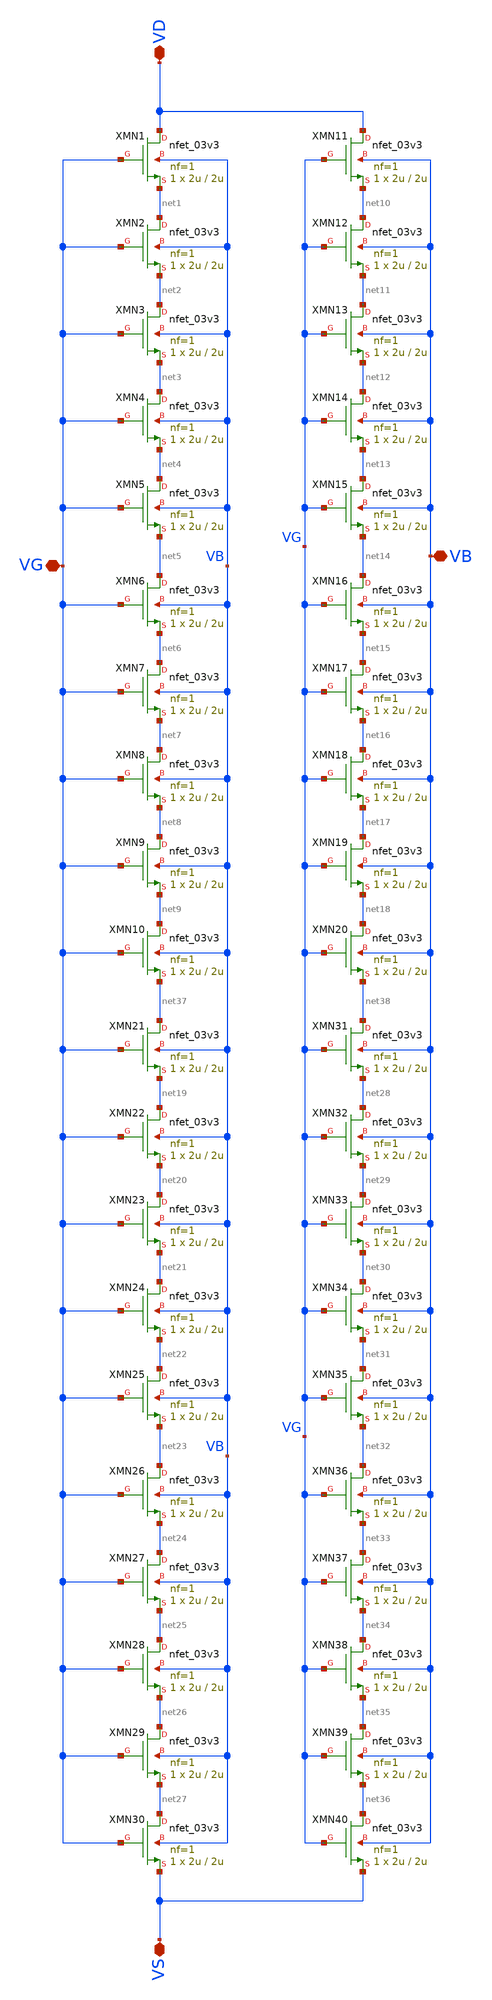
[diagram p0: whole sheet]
** sch_path: Voltage_Reference/symbols_vr/10_NMOS_series.sch
**.subckt 10_NMOS_series VD VG VS VB
*.iopin VD
*.iopin VG
*.iopin VS
*.iopin VB
XMN1 VD VG net1 VB nfet_03v3 L=2u W=2u nf=1 ad='int((nf+1)/2) * W/nf * 0.18u' as='int((nf+2)/2) * W/nf * 0.18u'
+ pd='2*int((nf+1)/2) * (W/nf + 0.18u)' ps='2*int((nf+2)/2) * (W/nf + 0.18u)' nrd='0.18u / W' nrs='0.18u / W'
+ sa=0 sb=0 sd=0 m=1
XMN2 net1 VG net2 VB nfet_03v3 L=2u W=2u nf=1 ad='int((nf+1)/2) * W/nf * 0.18u' as='int((nf+2)/2) * W/nf * 0.18u'
+ pd='2*int((nf+1)/2) * (W/nf + 0.18u)' ps='2*int((nf+2)/2) * (W/nf + 0.18u)' nrd='0.18u / W' nrs='0.18u / W'
+ sa=0 sb=0 sd=0 m=1
XMN3 net2 VG net3 VB nfet_03v3 L=2u W=2u nf=1 ad='int((nf+1)/2) * W/nf * 0.18u' as='int((nf+2)/2) * W/nf * 0.18u'
+ pd='2*int((nf+1)/2) * (W/nf + 0.18u)' ps='2*int((nf+2)/2) * (W/nf + 0.18u)' nrd='0.18u / W' nrs='0.18u / W'
+ sa=0 sb=0 sd=0 m=1
XMN4 net3 VG net4 VB nfet_03v3 L=2u W=2u nf=1 ad='int((nf+1)/2) * W/nf * 0.18u' as='int((nf+2)/2) * W/nf * 0.18u'
+ pd='2*int((nf+1)/2) * (W/nf + 0.18u)' ps='2*int((nf+2)/2) * (W/nf + 0.18u)' nrd='0.18u / W' nrs='0.18u / W'
+ sa=0 sb=0 sd=0 m=1
XMN5 net4 VG net5 VB nfet_03v3 L=2u W=2u nf=1 ad='int((nf+1)/2) * W/nf * 0.18u' as='int((nf+2)/2) * W/nf * 0.18u'
+ pd='2*int((nf+1)/2) * (W/nf + 0.18u)' ps='2*int((nf+2)/2) * (W/nf + 0.18u)' nrd='0.18u / W' nrs='0.18u / W'
+ sa=0 sb=0 sd=0 m=1
XMN6 net5 VG net6 VB nfet_03v3 L=2u W=2u nf=1 ad='int((nf+1)/2) * W/nf * 0.18u' as='int((nf+2)/2) * W/nf * 0.18u'
+ pd='2*int((nf+1)/2) * (W/nf + 0.18u)' ps='2*int((nf+2)/2) * (W/nf + 0.18u)' nrd='0.18u / W' nrs='0.18u / W'
+ sa=0 sb=0 sd=0 m=1
XMN7 net6 VG net7 VB nfet_03v3 L=2u W=2u nf=1 ad='int((nf+1)/2) * W/nf * 0.18u' as='int((nf+2)/2) * W/nf * 0.18u'
+ pd='2*int((nf+1)/2) * (W/nf + 0.18u)' ps='2*int((nf+2)/2) * (W/nf + 0.18u)' nrd='0.18u / W' nrs='0.18u / W'
+ sa=0 sb=0 sd=0 m=1
XMN8 net7 VG net8 VB nfet_03v3 L=2u W=2u nf=1 ad='int((nf+1)/2) * W/nf * 0.18u' as='int((nf+2)/2) * W/nf * 0.18u'
+ pd='2*int((nf+1)/2) * (W/nf + 0.18u)' ps='2*int((nf+2)/2) * (W/nf + 0.18u)' nrd='0.18u / W' nrs='0.18u / W'
+ sa=0 sb=0 sd=0 m=1
XMN9 net8 VG net9 VB nfet_03v3 L=2u W=2u nf=1 ad='int((nf+1)/2) * W/nf * 0.18u' as='int((nf+2)/2) * W/nf * 0.18u'
+ pd='2*int((nf+1)/2) * (W/nf + 0.18u)' ps='2*int((nf+2)/2) * (W/nf + 0.18u)' nrd='0.18u / W' nrs='0.18u / W'
+ sa=0 sb=0 sd=0 m=1
XMN10 net9 VG net37 VB nfet_03v3 L=2u W=2u nf=1 ad='int((nf+1)/2) * W/nf * 0.18u' as='int((nf+2)/2) * W/nf * 0.18u'
+ pd='2*int((nf+1)/2) * (W/nf + 0.18u)' ps='2*int((nf+2)/2) * (W/nf + 0.18u)' nrd='0.18u / W' nrs='0.18u / W'
+ sa=0 sb=0 sd=0 m=1
XMN11 VD VG net10 VB nfet_03v3 L=2u W=2u nf=1 ad='int((nf+1)/2) * W/nf * 0.18u' as='int((nf+2)/2) * W/nf * 0.18u'
+ pd='2*int((nf+1)/2) * (W/nf + 0.18u)' ps='2*int((nf+2)/2) * (W/nf + 0.18u)' nrd='0.18u / W' nrs='0.18u / W'
+ sa=0 sb=0 sd=0 m=1
XMN12 net10 VG net11 VB nfet_03v3 L=2u W=2u nf=1 ad='int((nf+1)/2) * W/nf * 0.18u' as='int((nf+2)/2) * W/nf * 0.18u'
+ pd='2*int((nf+1)/2) * (W/nf + 0.18u)' ps='2*int((nf+2)/2) * (W/nf + 0.18u)' nrd='0.18u / W' nrs='0.18u / W'
+ sa=0 sb=0 sd=0 m=1
XMN13 net11 VG net12 VB nfet_03v3 L=2u W=2u nf=1 ad='int((nf+1)/2) * W/nf * 0.18u' as='int((nf+2)/2) * W/nf * 0.18u'
+ pd='2*int((nf+1)/2) * (W/nf + 0.18u)' ps='2*int((nf+2)/2) * (W/nf + 0.18u)' nrd='0.18u / W' nrs='0.18u / W'
+ sa=0 sb=0 sd=0 m=1
XMN14 net12 VG net13 VB nfet_03v3 L=2u W=2u nf=1 ad='int((nf+1)/2) * W/nf * 0.18u' as='int((nf+2)/2) * W/nf * 0.18u'
+ pd='2*int((nf+1)/2) * (W/nf + 0.18u)' ps='2*int((nf+2)/2) * (W/nf + 0.18u)' nrd='0.18u / W' nrs='0.18u / W'
+ sa=0 sb=0 sd=0 m=1
XMN15 net13 VG net14 VB nfet_03v3 L=2u W=2u nf=1 ad='int((nf+1)/2) * W/nf * 0.18u' as='int((nf+2)/2) * W/nf * 0.18u'
+ pd='2*int((nf+1)/2) * (W/nf + 0.18u)' ps='2*int((nf+2)/2) * (W/nf + 0.18u)' nrd='0.18u / W' nrs='0.18u / W'
+ sa=0 sb=0 sd=0 m=1
XMN16 net14 VG net15 VB nfet_03v3 L=2u W=2u nf=1 ad='int((nf+1)/2) * W/nf * 0.18u' as='int((nf+2)/2) * W/nf * 0.18u'
+ pd='2*int((nf+1)/2) * (W/nf + 0.18u)' ps='2*int((nf+2)/2) * (W/nf + 0.18u)' nrd='0.18u / W' nrs='0.18u / W'
+ sa=0 sb=0 sd=0 m=1
XMN17 net15 VG net16 VB nfet_03v3 L=2u W=2u nf=1 ad='int((nf+1)/2) * W/nf * 0.18u' as='int((nf+2)/2) * W/nf * 0.18u'
+ pd='2*int((nf+1)/2) * (W/nf + 0.18u)' ps='2*int((nf+2)/2) * (W/nf + 0.18u)' nrd='0.18u / W' nrs='0.18u / W'
+ sa=0 sb=0 sd=0 m=1
XMN18 net16 VG net17 VB nfet_03v3 L=2u W=2u nf=1 ad='int((nf+1)/2) * W/nf * 0.18u' as='int((nf+2)/2) * W/nf * 0.18u'
+ pd='2*int((nf+1)/2) * (W/nf + 0.18u)' ps='2*int((nf+2)/2) * (W/nf + 0.18u)' nrd='0.18u / W' nrs='0.18u / W'
+ sa=0 sb=0 sd=0 m=1
XMN19 net17 VG net18 VB nfet_03v3 L=2u W=2u nf=1 ad='int((nf+1)/2) * W/nf * 0.18u' as='int((nf+2)/2) * W/nf * 0.18u'
+ pd='2*int((nf+1)/2) * (W/nf + 0.18u)' ps='2*int((nf+2)/2) * (W/nf + 0.18u)' nrd='0.18u / W' nrs='0.18u / W'
+ sa=0 sb=0 sd=0 m=1
XMN20 net18 VG net38 VB nfet_03v3 L=2u W=2u nf=1 ad='int((nf+1)/2) * W/nf * 0.18u' as='int((nf+2)/2) * W/nf * 0.18u'
+ pd='2*int((nf+1)/2) * (W/nf + 0.18u)' ps='2*int((nf+2)/2) * (W/nf + 0.18u)' nrd='0.18u / W' nrs='0.18u / W'
+ sa=0 sb=0 sd=0 m=1
XMN21 net37 VG net19 VB nfet_03v3 L=2u W=2u nf=1 ad='int((nf+1)/2) * W/nf * 0.18u' as='int((nf+2)/2) * W/nf * 0.18u'
+ pd='2*int((nf+1)/2) * (W/nf + 0.18u)' ps='2*int((nf+2)/2) * (W/nf + 0.18u)' nrd='0.18u / W' nrs='0.18u / W'
+ sa=0 sb=0 sd=0 m=1
XMN22 net19 VG net20 VB nfet_03v3 L=2u W=2u nf=1 ad='int((nf+1)/2) * W/nf * 0.18u' as='int((nf+2)/2) * W/nf * 0.18u'
+ pd='2*int((nf+1)/2) * (W/nf + 0.18u)' ps='2*int((nf+2)/2) * (W/nf + 0.18u)' nrd='0.18u / W' nrs='0.18u / W'
+ sa=0 sb=0 sd=0 m=1
XMN23 net20 VG net21 VB nfet_03v3 L=2u W=2u nf=1 ad='int((nf+1)/2) * W/nf * 0.18u' as='int((nf+2)/2) * W/nf * 0.18u'
+ pd='2*int((nf+1)/2) * (W/nf + 0.18u)' ps='2*int((nf+2)/2) * (W/nf + 0.18u)' nrd='0.18u / W' nrs='0.18u / W'
+ sa=0 sb=0 sd=0 m=1
XMN24 net21 VG net22 VB nfet_03v3 L=2u W=2u nf=1 ad='int((nf+1)/2) * W/nf * 0.18u' as='int((nf+2)/2) * W/nf * 0.18u'
+ pd='2*int((nf+1)/2) * (W/nf + 0.18u)' ps='2*int((nf+2)/2) * (W/nf + 0.18u)' nrd='0.18u / W' nrs='0.18u / W'
+ sa=0 sb=0 sd=0 m=1
XMN25 net22 VG net23 VB nfet_03v3 L=2u W=2u nf=1 ad='int((nf+1)/2) * W/nf * 0.18u' as='int((nf+2)/2) * W/nf * 0.18u'
+ pd='2*int((nf+1)/2) * (W/nf + 0.18u)' ps='2*int((nf+2)/2) * (W/nf + 0.18u)' nrd='0.18u / W' nrs='0.18u / W'
+ sa=0 sb=0 sd=0 m=1
XMN26 net23 VG net24 VB nfet_03v3 L=2u W=2u nf=1 ad='int((nf+1)/2) * W/nf * 0.18u' as='int((nf+2)/2) * W/nf * 0.18u'
+ pd='2*int((nf+1)/2) * (W/nf + 0.18u)' ps='2*int((nf+2)/2) * (W/nf + 0.18u)' nrd='0.18u / W' nrs='0.18u / W'
+ sa=0 sb=0 sd=0 m=1
XMN27 net24 VG net25 VB nfet_03v3 L=2u W=2u nf=1 ad='int((nf+1)/2) * W/nf * 0.18u' as='int((nf+2)/2) * W/nf * 0.18u'
+ pd='2*int((nf+1)/2) * (W/nf + 0.18u)' ps='2*int((nf+2)/2) * (W/nf + 0.18u)' nrd='0.18u / W' nrs='0.18u / W'
+ sa=0 sb=0 sd=0 m=1
XMN28 net25 VG net26 VB nfet_03v3 L=2u W=2u nf=1 ad='int((nf+1)/2) * W/nf * 0.18u' as='int((nf+2)/2) * W/nf * 0.18u'
+ pd='2*int((nf+1)/2) * (W/nf + 0.18u)' ps='2*int((nf+2)/2) * (W/nf + 0.18u)' nrd='0.18u / W' nrs='0.18u / W'
+ sa=0 sb=0 sd=0 m=1
XMN29 net26 VG net27 VB nfet_03v3 L=2u W=2u nf=1 ad='int((nf+1)/2) * W/nf * 0.18u' as='int((nf+2)/2) * W/nf * 0.18u'
+ pd='2*int((nf+1)/2) * (W/nf + 0.18u)' ps='2*int((nf+2)/2) * (W/nf + 0.18u)' nrd='0.18u / W' nrs='0.18u / W'
+ sa=0 sb=0 sd=0 m=1
XMN30 net27 VG VS VB nfet_03v3 L=2u W=2u nf=1 ad='int((nf+1)/2) * W/nf * 0.18u' as='int((nf+2)/2) * W/nf * 0.18u'
+ pd='2*int((nf+1)/2) * (W/nf + 0.18u)' ps='2*int((nf+2)/2) * (W/nf + 0.18u)' nrd='0.18u / W' nrs='0.18u / W'
+ sa=0 sb=0 sd=0 m=1
XMN31 net38 VG net28 VB nfet_03v3 L=2u W=2u nf=1 ad='int((nf+1)/2) * W/nf * 0.18u' as='int((nf+2)/2) * W/nf * 0.18u'
+ pd='2*int((nf+1)/2) * (W/nf + 0.18u)' ps='2*int((nf+2)/2) * (W/nf + 0.18u)' nrd='0.18u / W' nrs='0.18u / W'
+ sa=0 sb=0 sd=0 m=1
XMN32 net28 VG net29 VB nfet_03v3 L=2u W=2u nf=1 ad='int((nf+1)/2) * W/nf * 0.18u' as='int((nf+2)/2) * W/nf * 0.18u'
+ pd='2*int((nf+1)/2) * (W/nf + 0.18u)' ps='2*int((nf+2)/2) * (W/nf + 0.18u)' nrd='0.18u / W' nrs='0.18u / W'
+ sa=0 sb=0 sd=0 m=1
XMN33 net29 VG net30 VB nfet_03v3 L=2u W=2u nf=1 ad='int((nf+1)/2) * W/nf * 0.18u' as='int((nf+2)/2) * W/nf * 0.18u'
+ pd='2*int((nf+1)/2) * (W/nf + 0.18u)' ps='2*int((nf+2)/2) * (W/nf + 0.18u)' nrd='0.18u / W' nrs='0.18u / W'
+ sa=0 sb=0 sd=0 m=1
XMN34 net30 VG net31 VB nfet_03v3 L=2u W=2u nf=1 ad='int((nf+1)/2) * W/nf * 0.18u' as='int((nf+2)/2) * W/nf * 0.18u'
+ pd='2*int((nf+1)/2) * (W/nf + 0.18u)' ps='2*int((nf+2)/2) * (W/nf + 0.18u)' nrd='0.18u / W' nrs='0.18u / W'
+ sa=0 sb=0 sd=0 m=1
XMN35 net31 VG net32 VB nfet_03v3 L=2u W=2u nf=1 ad='int((nf+1)/2) * W/nf * 0.18u' as='int((nf+2)/2) * W/nf * 0.18u'
+ pd='2*int((nf+1)/2) * (W/nf + 0.18u)' ps='2*int((nf+2)/2) * (W/nf + 0.18u)' nrd='0.18u / W' nrs='0.18u / W'
+ sa=0 sb=0 sd=0 m=1
XMN36 net32 VG net33 VB nfet_03v3 L=2u W=2u nf=1 ad='int((nf+1)/2) * W/nf * 0.18u' as='int((nf+2)/2) * W/nf * 0.18u'
+ pd='2*int((nf+1)/2) * (W/nf + 0.18u)' ps='2*int((nf+2)/2) * (W/nf + 0.18u)' nrd='0.18u / W' nrs='0.18u / W'
+ sa=0 sb=0 sd=0 m=1
XMN37 net33 VG net34 VB nfet_03v3 L=2u W=2u nf=1 ad='int((nf+1)/2) * W/nf * 0.18u' as='int((nf+2)/2) * W/nf * 0.18u'
+ pd='2*int((nf+1)/2) * (W/nf + 0.18u)' ps='2*int((nf+2)/2) * (W/nf + 0.18u)' nrd='0.18u / W' nrs='0.18u / W'
+ sa=0 sb=0 sd=0 m=1
XMN38 net34 VG net35 VB nfet_03v3 L=2u W=2u nf=1 ad='int((nf+1)/2) * W/nf * 0.18u' as='int((nf+2)/2) * W/nf * 0.18u'
+ pd='2*int((nf+1)/2) * (W/nf + 0.18u)' ps='2*int((nf+2)/2) * (W/nf + 0.18u)' nrd='0.18u / W' nrs='0.18u / W'
+ sa=0 sb=0 sd=0 m=1
XMN39 net35 VG net36 VB nfet_03v3 L=2u W=2u nf=1 ad='int((nf+1)/2) * W/nf * 0.18u' as='int((nf+2)/2) * W/nf * 0.18u'
+ pd='2*int((nf+1)/2) * (W/nf + 0.18u)' ps='2*int((nf+2)/2) * (W/nf + 0.18u)' nrd='0.18u / W' nrs='0.18u / W'
+ sa=0 sb=0 sd=0 m=1
XMN40 net36 VG VS VB nfet_03v3 L=2u W=2u nf=1 ad='int((nf+1)/2) * W/nf * 0.18u' as='int((nf+2)/2) * W/nf * 0.18u'
+ pd='2*int((nf+1)/2) * (W/nf + 0.18u)' ps='2*int((nf+2)/2) * (W/nf + 0.18u)' nrd='0.18u / W' nrs='0.18u / W'
+ sa=0 sb=0 sd=0 m=1
**.ends
.end
